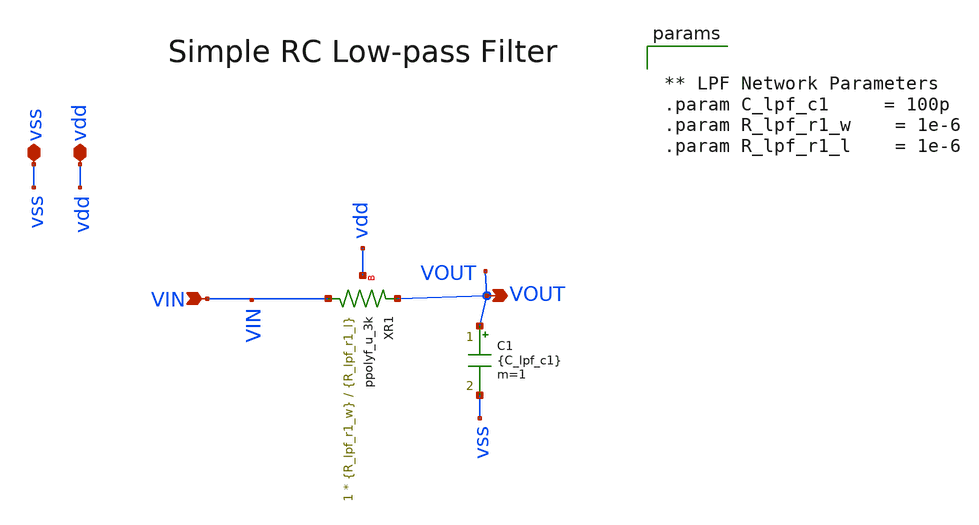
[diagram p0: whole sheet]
** sch_path: analog-db/circuits/ldo_005_buffered_ref/reference/ti-ldo/lpf/lpf_rc.sch
**.subckt lpf_rc VIN vdd vss VOUT
*.ipin VIN
*.iopin vdd
*.iopin vss
*.opin VOUT
XR1 VIN VOUT vdd ppolyf_u_3k r_width={R_lpf_r1_w} r_length={R_lpf_r1_l} m=1
C1 VOUT vss {C_lpf_c1} m=1
**** begin user architecture code

** LPF Network Parameters
.param C_lpf_c1 	= 100p
.param R_lpf_r1_w	= 1e-6
.param R_lpf_r1_l	= 1e-6


**** end user architecture code
**.ends
.end
